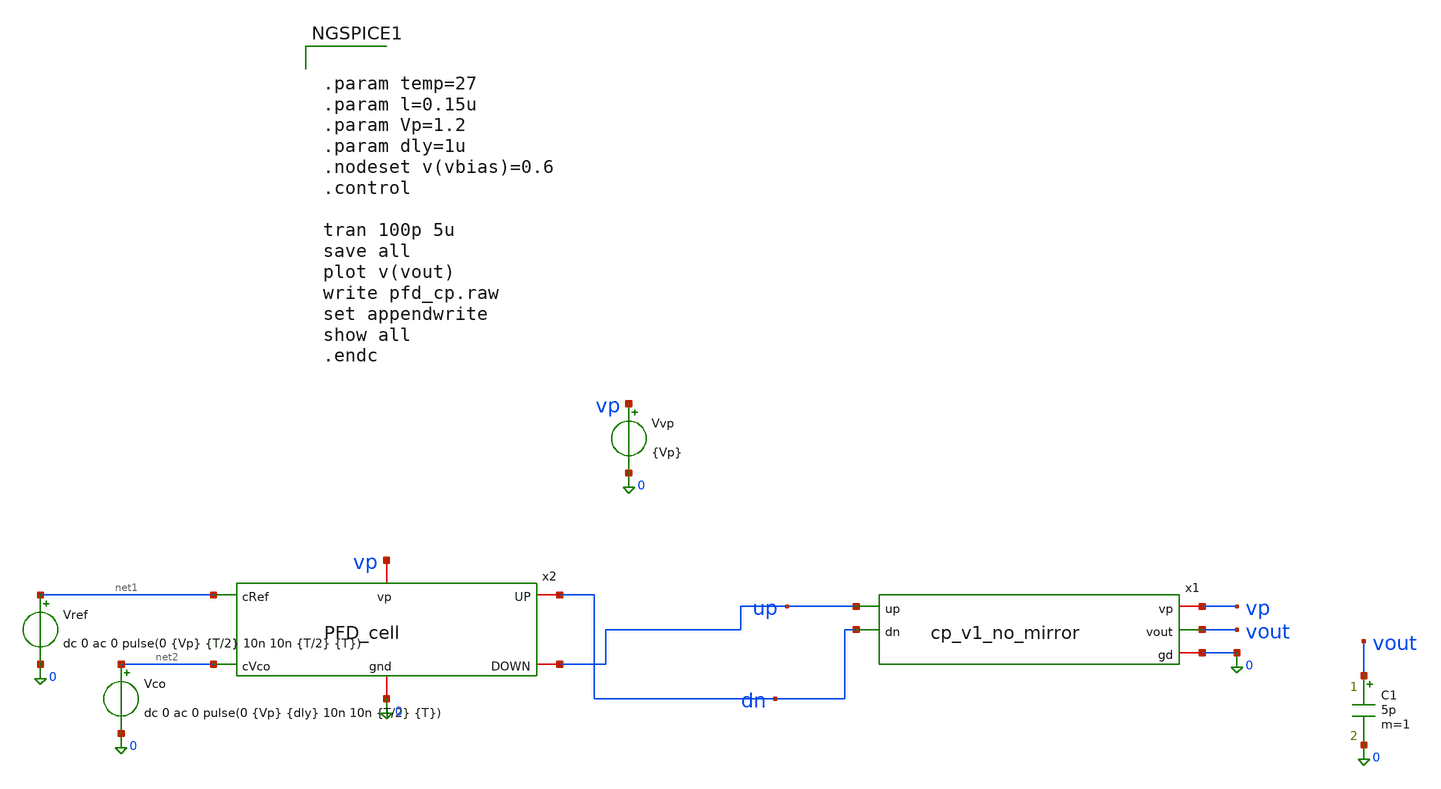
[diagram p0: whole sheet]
** sch_path: PLL0663-main/testbenches/tran/xschem/charge_pump/pfd_cp_tb.sch
**.subckt pfd_cp_tb
x1 vp up vout dn 0 cp_v1_no_mirror
Vvp vp 0 {Vp}
x2 0 vp net1 dn up net2 PFD_cell
Vco net2 0 dc 0 ac 0 pulse(0 {Vp} {dly} 10n 10n {T/2} {T})
Vref net1 0 dc 0 ac 0 pulse(0 {Vp} {T/2} 10n 10n {T/2} {T})
C1 vout 0 5p m=1
**** begin user architecture code


.param temp=27
.param l=0.15u
.param Vp=1.2
.param dly=1u
.nodeset v(vbias)=0.6
.control

tran 100p 5u
save all
plot v(vout)
write pfd_cp.raw
set appendwrite
show all
.endc


**** end user architecture code
**.ends
.end
